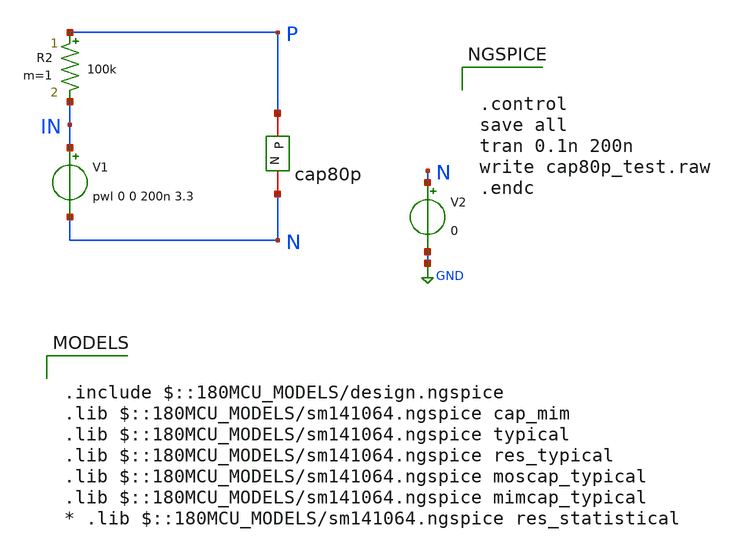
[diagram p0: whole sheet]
** sch_path: Clock_Generator_PAKISTAN_02/Schematics/cap80p_test.sch
**.subckt cap80p_test
V1 IN N pwl 0 0 200n 3.3
R2 P IN 100k m=1
x1 N P cap80p
V2 N GND 0
**** begin user architecture code

.include $::180MCU_MODELS/design.ngspice
.lib $::180MCU_MODELS/sm141064.ngspice cap_mim
.lib $::180MCU_MODELS/sm141064.ngspice typical
.lib $::180MCU_MODELS/sm141064.ngspice res_typical
.lib $::180MCU_MODELS/sm141064.ngspice moscap_typical
.lib $::180MCU_MODELS/sm141064.ngspice mimcap_typical
* .lib $::180MCU_MODELS/sm141064.ngspice res_statistical



.control
save all
tran 0.1n 200n
write cap80p_test.raw
.endc


**** end user architecture code
**.ends

* expanding   symbol:  cap80p.sym # of pins=2
** sym_path: Clock_Generator_PAKISTAN_02/xschem/cap80p.sym
** sch_path: Clock_Generator_PAKISTAN_02/xschem/cap80p.sch
.subckt cap80p N P
*.iopin P
*.iopin N
XC1 P N cap_mim_2f0_m4m5_noshield c_width=25e-6 c_length=25e-6 m=64
.ends

.GLOBAL GND
.end
